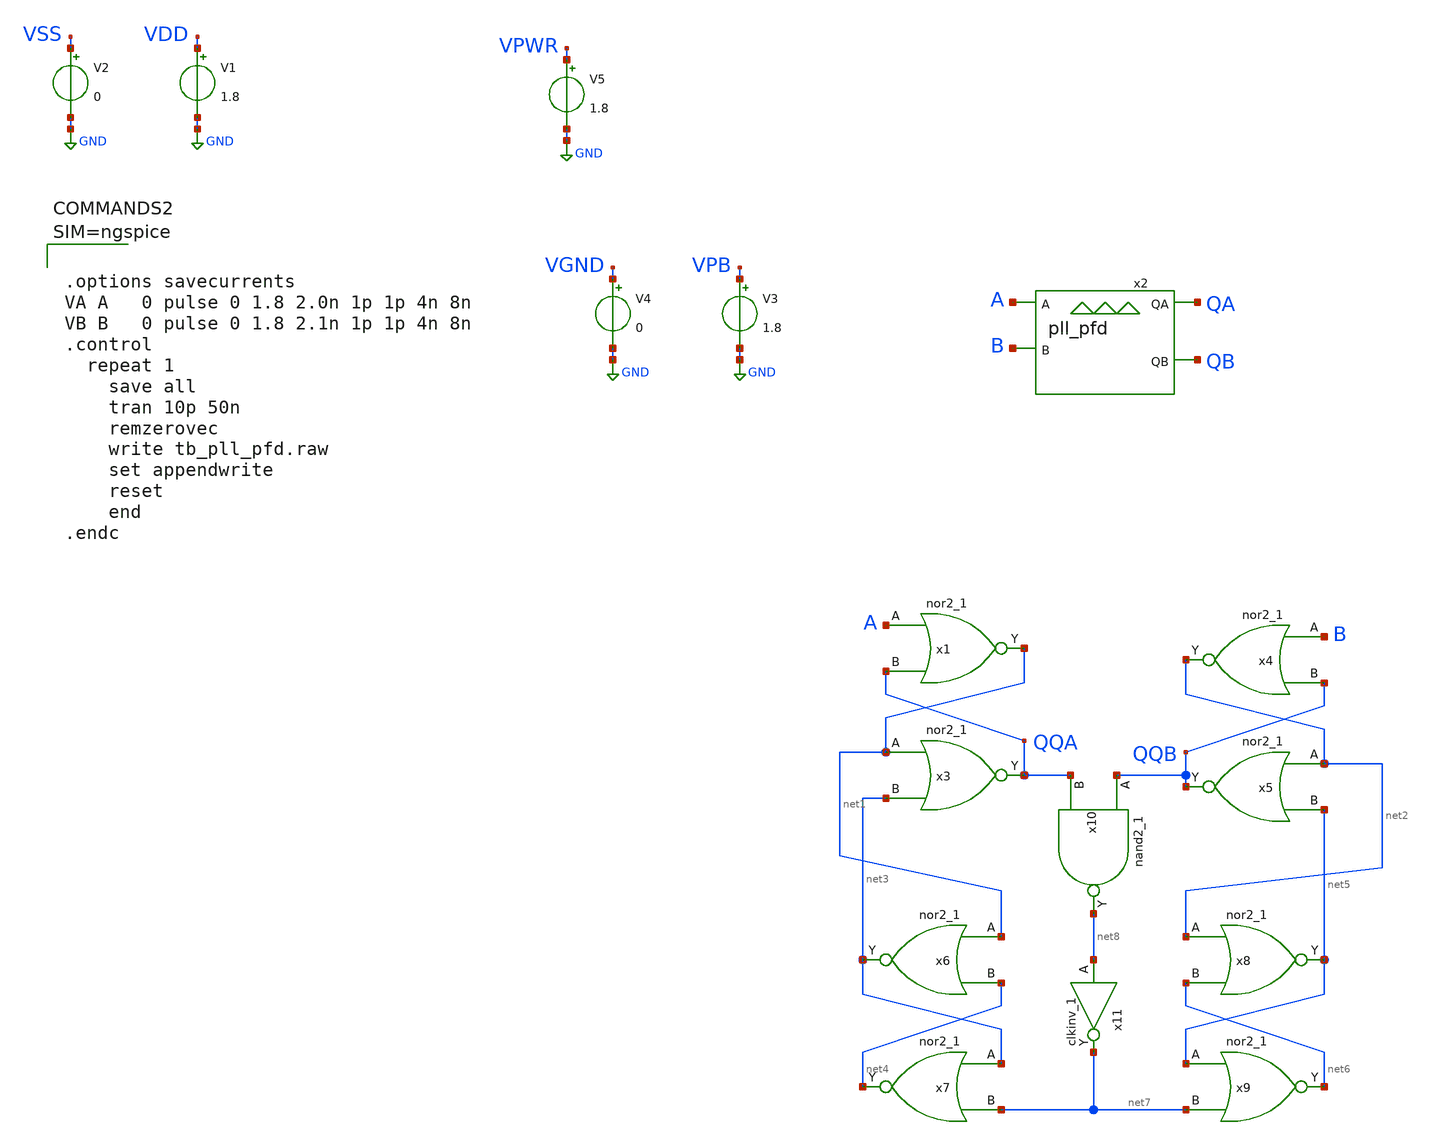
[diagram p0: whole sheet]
** sch_path: xschem/tb_pll_pfd.sch
**.subckt tb_pll_pfd
V1 VDD GND 1.8
V2 VSS GND 0
V5 VPWR GND 1.8
x2 A B QA QB VSS VSS VDD VDD pll_pfd
x1 A QQA VGND VNB VPB VPWR net1 sky130_fd_sc_hd__nor2_1
x3 net1 net3 VGND VNB VPB VPWR QQA sky130_fd_sc_hd__nor2_1
V3 VPB GND 1.8
V4 VGND GND 0
x4 B QQB VGND VNB VPB VPWR net2 sky130_fd_sc_hd__nor2_1
x5 net2 net5 VGND VNB VPB VPWR QQB sky130_fd_sc_hd__nor2_1
x6 net1 net4 VGND VNB VPB VPWR net3 sky130_fd_sc_hd__nor2_1
x7 net3 net7 VGND VNB VPB VPWR net4 sky130_fd_sc_hd__nor2_1
x8 net2 net6 VGND VNB VPB VPWR net5 sky130_fd_sc_hd__nor2_1
x9 net5 net7 VGND VNB VPB VPWR net6 sky130_fd_sc_hd__nor2_1
x10 QQB QQA VGND VNB VPB VPWR net8 sky130_fd_sc_hd__nand2_1
x11 net8 VGND VNB VPB VPWR net7 sky130_fd_sc_hd__clkinv_1
**** begin user architecture code

** opencircuitdesign pdks install
.lib $::SKYWATER_MODELS/sky130.lib.spice tt_mm
.include $::SKYWATER_STDCELLS/sky130_fd_sc_hd.spice





.options savecurrents
VA A   0 pulse 0 1.8 2.0n 1p 1p 4n 8n
VB B   0 pulse 0 1.8 2.1n 1p 1p 4n 8n
.control
  repeat 1
    save all
    tran 10p 50n
    remzerovec
    write tb_pll_pfd.raw
    set appendwrite
    reset
    end
.endc



**** end user architecture code
**.ends

* expanding   symbol:  pll_pfd.sym # of pins=4
** sym_path: xschem/pll_pfd.sym
** sch_path: xschem/pll_pfd.sch
.subckt pll_pfd A B QA QB VSS VNB VPB VDD
*.ipin A
*.ipin B
*.ipin VDD
*.ipin VPB
*.ipin VNB
*.ipin VSS
*.opin QA
*.opin QB
x1 QA A VPB VNB VDD QAB VSS pll_nor
x2 QAB RA VPB VNB VDD QA VSS pll_nor
x5 QB QA VPB VNB VDD VSS net3 pll_nand
x3 QB B VPB VNB VDD QBB VSS pll_nor
x4 QBB RB VPB VNB VDD QB VSS pll_nor
x6 net1 QAB VPB VNB VDD RA VSS pll_nor
x7 RA R VPB VNB VDD net1 VSS pll_nor
x8 net2 QBB VPB VNB VDD RB VSS pll_nor
x9 RB R VPB VNB VDD net2 VSS pll_nor
x10 net3 R VDD VSS pll_inv1
.ends


* expanding   symbol:  pll_nor.sym # of pins=7
** sym_path: xschem/pll_nor.sym
** sch_path: xschem/pll_nor.sch
.subckt pll_nor A B VPB VNB VDD Q VSS
*.opin Q
*.ipin A
*.ipin B
*.ipin VDD
*.ipin VPB
*.ipin VNB
*.ipin VSS
XM3 net1 A net2 VPB sky130_fd_pr__pfet_01v8_lvt L=0.35 W=1 nf=1 ad='int((nf+1)/2) * W/nf * 0.29' as='int((nf+2)/2) * W/nf * 0.29'
+ pd='2*int((nf+1)/2) * (W/nf + 0.29)' ps='2*int((nf+2)/2) * (W/nf + 0.29)' nrd='0.29 / W' nrs='0.29 / W'
+ sa=0 sb=0 sd=0 mult=1 m=1
vpwr VDD net2 0
.save i(vpwr)
XM1 Q A VSS VNB sky130_fd_pr__nfet_01v8_lvt L=0.25 W=0.5 nf=1 ad='int((nf+1)/2) * W/nf * 0.29' as='int((nf+2)/2) * W/nf * 0.29'
+ pd='2*int((nf+1)/2) * (W/nf + 0.29)' ps='2*int((nf+2)/2) * (W/nf + 0.29)' nrd='0.29 / W' nrs='0.29 / W'
+ sa=0 sb=0 sd=0 mult=1 m=1
XM2 Q B net1 VPB sky130_fd_pr__pfet_01v8_lvt L=0.35 W=1 nf=1 ad='int((nf+1)/2) * W/nf * 0.29' as='int((nf+2)/2) * W/nf * 0.29'
+ pd='2*int((nf+1)/2) * (W/nf + 0.29)' ps='2*int((nf+2)/2) * (W/nf + 0.29)' nrd='0.29 / W' nrs='0.29 / W'
+ sa=0 sb=0 sd=0 mult=1 m=1
XM4 Q B VSS VNB sky130_fd_pr__nfet_01v8_lvt L=0.25 W=0.5 nf=1 ad='int((nf+1)/2) * W/nf * 0.29' as='int((nf+2)/2) * W/nf * 0.29'
+ pd='2*int((nf+1)/2) * (W/nf + 0.29)' ps='2*int((nf+2)/2) * (W/nf + 0.29)' nrd='0.29 / W' nrs='0.29 / W'
+ sa=0 sb=0 sd=0 mult=1 m=1
.ends


* expanding   symbol:  pll_nand.sym # of pins=7
** sym_path: xschem/pll_nand.sym
** sch_path: xschem/pll_nand.sch
.subckt pll_nand A B VPB VNB VDD VSS Q
*.opin Q
*.ipin A
*.ipin B
*.ipin VDD
*.ipin VPB
*.ipin VNB
*.ipin VSS
XM3 Q B net2 VPB sky130_fd_pr__pfet_01v8_lvt L=0.35 W=1 nf=1 ad='int((nf+1)/2) * W/nf * 0.29' as='int((nf+2)/2) * W/nf * 0.29'
+ pd='2*int((nf+1)/2) * (W/nf + 0.29)' ps='2*int((nf+2)/2) * (W/nf + 0.29)' nrd='0.29 / W' nrs='0.29 / W'
+ sa=0 sb=0 sd=0 mult=1 m=1
vpwr VDD net2 0
.save i(vpwr)
XM1 net1 B VSS VNB sky130_fd_pr__nfet_01v8_lvt L=0.25 W=0.5 nf=1 ad='int((nf+1)/2) * W/nf * 0.29' as='int((nf+2)/2) * W/nf * 0.29'
+ pd='2*int((nf+1)/2) * (W/nf + 0.29)' ps='2*int((nf+2)/2) * (W/nf + 0.29)' nrd='0.29 / W' nrs='0.29 / W'
+ sa=0 sb=0 sd=0 mult=1 m=1
XM2 Q A net2 VPB sky130_fd_pr__pfet_01v8_lvt L=0.35 W=1 nf=1 ad='int((nf+1)/2) * W/nf * 0.29' as='int((nf+2)/2) * W/nf * 0.29'
+ pd='2*int((nf+1)/2) * (W/nf + 0.29)' ps='2*int((nf+2)/2) * (W/nf + 0.29)' nrd='0.29 / W' nrs='0.29 / W'
+ sa=0 sb=0 sd=0 mult=1 m=1
XM4 Q A net1 VNB sky130_fd_pr__nfet_01v8_lvt L=0.25 W=0.5 nf=1 ad='int((nf+1)/2) * W/nf * 0.29' as='int((nf+2)/2) * W/nf * 0.29'
+ pd='2*int((nf+1)/2) * (W/nf + 0.29)' ps='2*int((nf+2)/2) * (W/nf + 0.29)' nrd='0.29 / W' nrs='0.29 / W'
+ sa=0 sb=0 sd=0 mult=1 m=1
.ends


* expanding   symbol:  pll_inv1.sym # of pins=2
** sym_path: xschem/pll_inv1.sym
** sch_path: xschem/pll_inv1.sch
.subckt pll_inv1 D Q VDD VSS
*.opin Q
*.ipin D
*.ipin VDD
*.ipin VSS
XM3 Q D net1 net1 sky130_fd_pr__pfet_01v8_lvt L=0.5 W=1 nf=1 ad='int((nf+1)/2) * W/nf * 0.29' as='int((nf+2)/2) * W/nf * 0.29'
+ pd='2*int((nf+1)/2) * (W/nf + 0.29)' ps='2*int((nf+2)/2) * (W/nf + 0.29)' nrd='0.29 / W' nrs='0.29 / W'
+ sa=0 sb=0 sd=0 mult=1 m=1
vpwr VDD net1 0
.save i(vpwr)
XM1 Q D VSS VSS sky130_fd_pr__nfet_01v8_lvt L=0.25 W=0.5 nf=1 ad='int((nf+1)/2) * W/nf * 0.29' as='int((nf+2)/2) * W/nf * 0.29'
+ pd='2*int((nf+1)/2) * (W/nf + 0.29)' ps='2*int((nf+2)/2) * (W/nf + 0.29)' nrd='0.29 / W' nrs='0.29 / W'
+ sa=0 sb=0 sd=0 mult=1 m=1
.ends

.GLOBAL GND
.end
